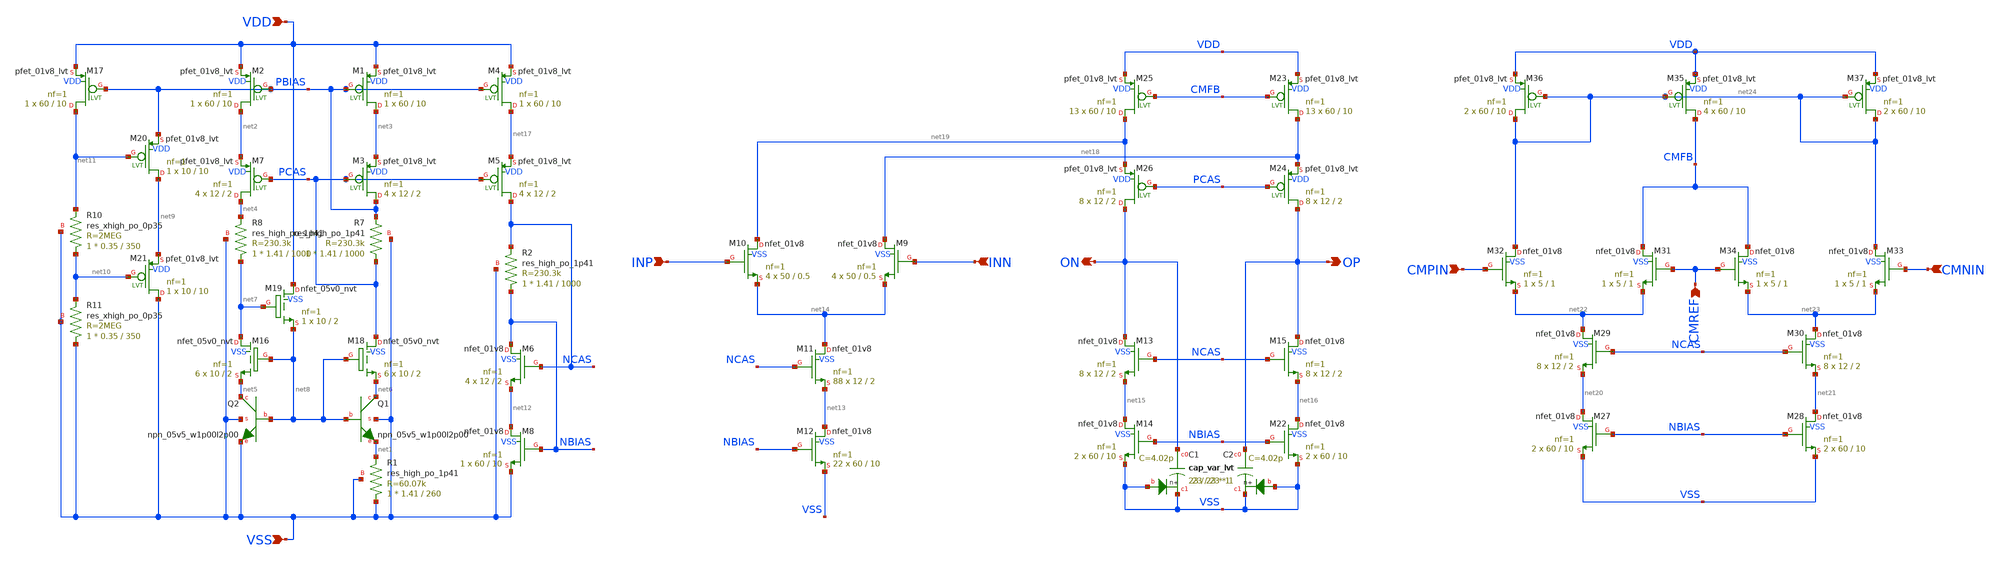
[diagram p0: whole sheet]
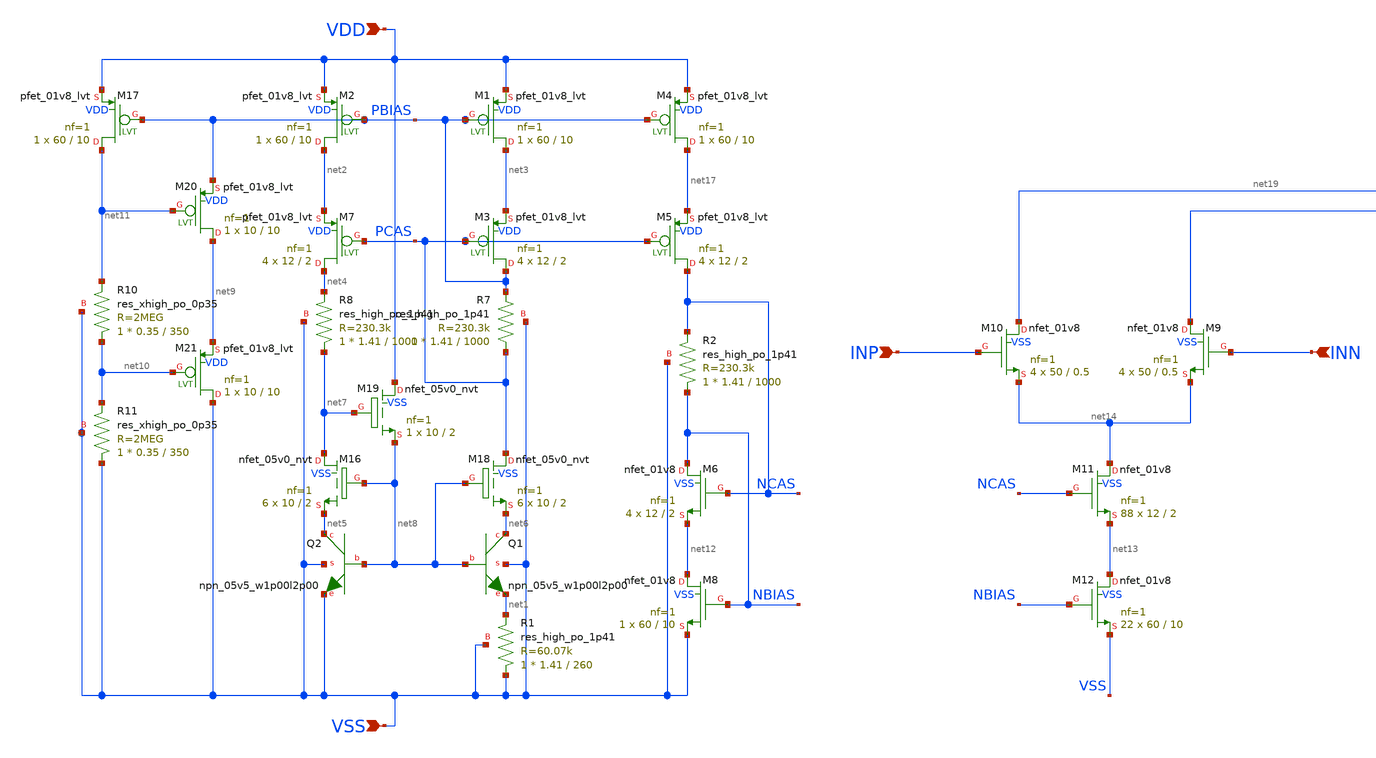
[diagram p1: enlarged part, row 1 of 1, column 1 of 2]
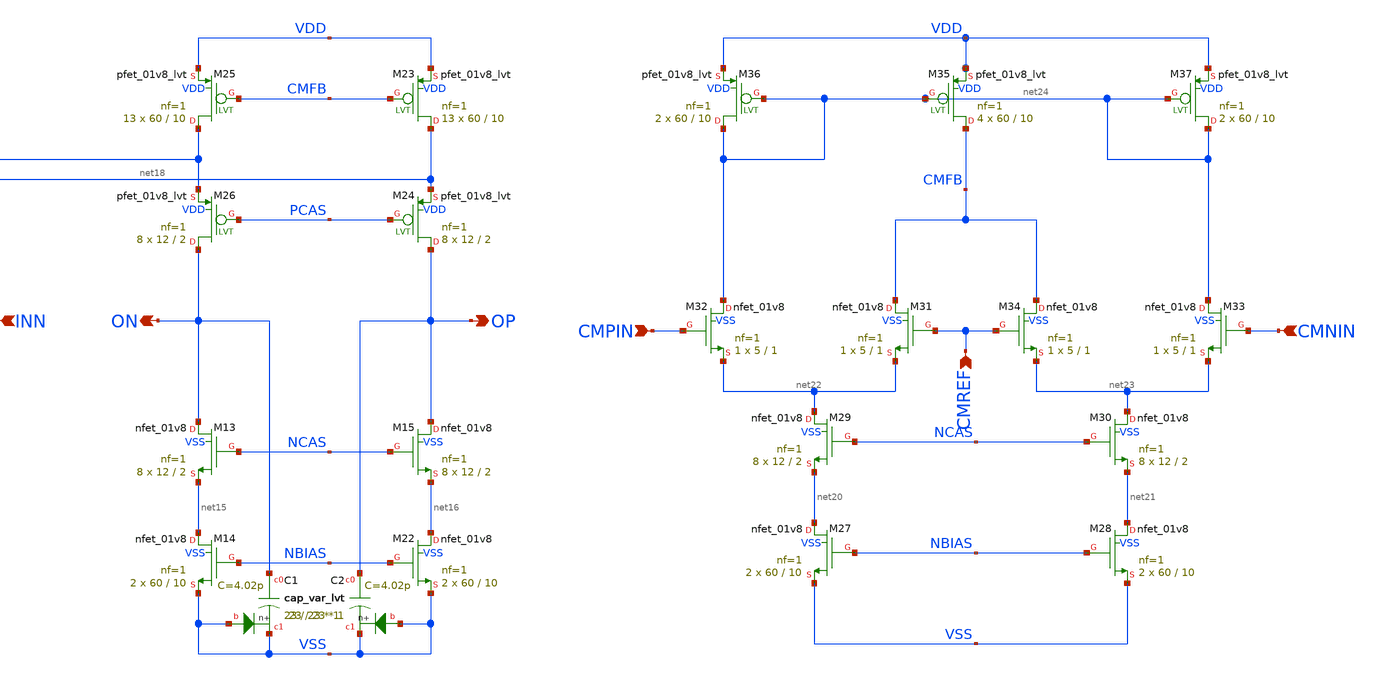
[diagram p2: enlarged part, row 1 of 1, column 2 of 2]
** sch_path: designs/fully_differential_amplifier.sch
**.subckt fully_differential_amplifier INP INN VDD VSS OP ON CMPIN CMNIN CMREF
*.ipin INP
*.ipin INN
*.ipin VDD
*.ipin VSS
*.opin OP
*.opin ON
*.ipin CMPIN
*.ipin CMNIN
*.ipin CMREF
XM1 net3 PBIAS VDD VDD sky130_fd_pr__pfet_01v8_lvt L=10 W=60 nf=1 ad='int((nf+1)/2) * W/nf * 0.29' as='int((nf+2)/2) * W/nf * 0.29'
+ pd='2*int((nf+1)/2) * (W/nf + 0.29)' ps='2*int((nf+2)/2) * (W/nf + 0.29)' nrd='0.29 / W' nrs='0.29 / W'
+ sa=0 sb=0 sd=0 mult=1 m=1
XM2 net2 PBIAS VDD VDD sky130_fd_pr__pfet_01v8_lvt L=10 W=60 nf=1 ad='int((nf+1)/2) * W/nf * 0.29' as='int((nf+2)/2) * W/nf * 0.29'
+ pd='2*int((nf+1)/2) * (W/nf + 0.29)' ps='2*int((nf+2)/2) * (W/nf + 0.29)' nrd='0.29 / W' nrs='0.29 / W'
+ sa=0 sb=0 sd=0 mult=1 m=1
XQ1 net6 net8 net1 VSS sky130_fd_pr__npn_05v5_w1p00l2p00
XQ2 net5 net8 VSS VSS sky130_fd_pr__npn_05v5_w1p00l2p00
XR1 VSS net1 VSS sky130_fd_pr__res_high_po_1p41 L=260 mult=1 m=1
XM3 PBIAS PCAS net3 VDD sky130_fd_pr__pfet_01v8_lvt L=2 W=12 nf=1 ad='int((nf+1)/2) * W/nf * 0.29' as='int((nf+2)/2) * W/nf * 0.29'
+ pd='2*int((nf+1)/2) * (W/nf + 0.29)' ps='2*int((nf+2)/2) * (W/nf + 0.29)' nrd='0.29 / W' nrs='0.29 / W'
+ sa=0 sb=0 sd=0 mult=4 m=4
XM7 net4 PCAS net2 VDD sky130_fd_pr__pfet_01v8_lvt L=2 W=12 nf=1 ad='int((nf+1)/2) * W/nf * 0.29' as='int((nf+2)/2) * W/nf * 0.29'
+ pd='2*int((nf+1)/2) * (W/nf + 0.29)' ps='2*int((nf+2)/2) * (W/nf + 0.29)' nrd='0.29 / W' nrs='0.29 / W'
+ sa=0 sb=0 sd=0 mult=4 m=4
XR7 PCAS PBIAS VSS sky130_fd_pr__res_high_po_1p41 L=1000 mult=1 m=1
XR8 net7 net4 VSS sky130_fd_pr__res_high_po_1p41 L=1000 mult=1 m=1
XM16 net7 net8 net5 VSS sky130_fd_pr__nfet_05v0_nvt L=2 W=10 nf=1 ad='int((nf+1)/2) * W/nf * 0.29' as='int((nf+2)/2) * W/nf * 0.29'
+ pd='2*int((nf+1)/2) * (W/nf + 0.29)' ps='2*int((nf+2)/2) * (W/nf + 0.29)' nrd='0.29 / W' nrs='0.29 / W'
+ sa=0 sb=0 sd=0 mult=6 m=6
XM18 PCAS net8 net6 VSS sky130_fd_pr__nfet_05v0_nvt L=2 W=10 nf=1 ad='int((nf+1)/2) * W/nf * 0.29' as='int((nf+2)/2) * W/nf * 0.29'
+ pd='2*int((nf+1)/2) * (W/nf + 0.29)' ps='2*int((nf+2)/2) * (W/nf + 0.29)' nrd='0.29 / W' nrs='0.29 / W'
+ sa=0 sb=0 sd=0 mult=6 m=6
XM19 VDD net7 net8 VSS sky130_fd_pr__nfet_05v0_nvt L=2 W=10 nf=1 ad='int((nf+1)/2) * W/nf * 0.29' as='int((nf+2)/2) * W/nf * 0.29'
+ pd='2*int((nf+1)/2) * (W/nf + 0.29)' ps='2*int((nf+2)/2) * (W/nf + 0.29)' nrd='0.29 / W' nrs='0.29 / W'
+ sa=0 sb=0 sd=0 mult=1 m=1
XM17 net11 PBIAS VDD VDD sky130_fd_pr__pfet_01v8_lvt L=10 W=60 nf=1 ad='int((nf+1)/2) * W/nf * 0.29'
+ as='int((nf+2)/2) * W/nf * 0.29' pd='2*int((nf+1)/2) * (W/nf + 0.29)' ps='2*int((nf+2)/2) * (W/nf + 0.29)'
+ nrd='0.29 / W' nrs='0.29 / W' sa=0 sb=0 sd=0 mult=1 m=1
XM20 net9 net11 PBIAS VDD sky130_fd_pr__pfet_01v8_lvt L=10 W=10 nf=1 ad='int((nf+1)/2) * W/nf * 0.29'
+ as='int((nf+2)/2) * W/nf * 0.29' pd='2*int((nf+1)/2) * (W/nf + 0.29)' ps='2*int((nf+2)/2) * (W/nf + 0.29)'
+ nrd='0.29 / W' nrs='0.29 / W' sa=0 sb=0 sd=0 mult=1 m=1
XM21 VSS net10 net9 VDD sky130_fd_pr__pfet_01v8_lvt L=10 W=10 nf=1 ad='int((nf+1)/2) * W/nf * 0.29' as='int((nf+2)/2) * W/nf * 0.29'
+ pd='2*int((nf+1)/2) * (W/nf + 0.29)' ps='2*int((nf+2)/2) * (W/nf + 0.29)' nrd='0.29 / W' nrs='0.29 / W'
+ sa=0 sb=0 sd=0 mult=1 m=1
XR10 net10 net11 VSS sky130_fd_pr__res_xhigh_po_0p35 L=350 mult=1 m=1
XR11 VSS net10 VSS sky130_fd_pr__res_xhigh_po_0p35 L=350 mult=1 m=1
XM4 net17 PBIAS VDD VDD sky130_fd_pr__pfet_01v8_lvt L=10 W=60 nf=1 ad='int((nf+1)/2) * W/nf * 0.29' as='int((nf+2)/2) * W/nf * 0.29'
+ pd='2*int((nf+1)/2) * (W/nf + 0.29)' ps='2*int((nf+2)/2) * (W/nf + 0.29)' nrd='0.29 / W' nrs='0.29 / W'
+ sa=0 sb=0 sd=0 mult=1 m=1
XM5 NCAS PCAS net17 VDD sky130_fd_pr__pfet_01v8_lvt L=2 W=12 nf=1 ad='int((nf+1)/2) * W/nf * 0.29' as='int((nf+2)/2) * W/nf * 0.29'
+ pd='2*int((nf+1)/2) * (W/nf + 0.29)' ps='2*int((nf+2)/2) * (W/nf + 0.29)' nrd='0.29 / W' nrs='0.29 / W'
+ sa=0 sb=0 sd=0 mult=4 m=4
XR2 NBIAS NCAS VSS sky130_fd_pr__res_high_po_1p41 L=1000 mult=1 m=1
XM6 NBIAS NCAS net12 VSS sky130_fd_pr__nfet_01v8 L=2 W=12 nf=1 ad='int((nf+1)/2) * W/nf * 0.29' as='int((nf+2)/2) * W/nf * 0.29'
+ pd='2*int((nf+1)/2) * (W/nf + 0.29)' ps='2*int((nf+2)/2) * (W/nf + 0.29)' nrd='0.29 / W' nrs='0.29 / W'
+ sa=0 sb=0 sd=0 mult=4 m=4
XM8 net12 NBIAS VSS VSS sky130_fd_pr__nfet_01v8 L=10 W=60 nf=1 ad='int((nf+1)/2) * W/nf * 0.29' as='int((nf+2)/2) * W/nf * 0.29'
+ pd='2*int((nf+1)/2) * (W/nf + 0.29)' ps='2*int((nf+2)/2) * (W/nf + 0.29)' nrd='0.29 / W' nrs='0.29 / W'
+ sa=0 sb=0 sd=0 mult=1 m=1
XM9 net18 INN net14 VSS sky130_fd_pr__nfet_01v8 L=0.5 W=50 nf=1 ad='int((nf+1)/2) * W/nf * 0.29' as='int((nf+2)/2) * W/nf * 0.29'
+ pd='2*int((nf+1)/2) * (W/nf + 0.29)' ps='2*int((nf+2)/2) * (W/nf + 0.29)' nrd='0.29 / W' nrs='0.29 / W'
+ sa=0 sb=0 sd=0 mult=4 m=4
XM10 net19 INP net14 VSS sky130_fd_pr__nfet_01v8 L=0.5 W=50 nf=1 ad='int((nf+1)/2) * W/nf * 0.29' as='int((nf+2)/2) * W/nf * 0.29'
+ pd='2*int((nf+1)/2) * (W/nf + 0.29)' ps='2*int((nf+2)/2) * (W/nf + 0.29)' nrd='0.29 / W' nrs='0.29 / W'
+ sa=0 sb=0 sd=0 mult=4 m=4
XM11 net14 NCAS net13 VSS sky130_fd_pr__nfet_01v8 L=2 W=12 nf=1 ad='int((nf+1)/2) * W/nf * 0.29' as='int((nf+2)/2) * W/nf * 0.29'
+ pd='2*int((nf+1)/2) * (W/nf + 0.29)' ps='2*int((nf+2)/2) * (W/nf + 0.29)' nrd='0.29 / W' nrs='0.29 / W'
+ sa=0 sb=0 sd=0 mult=88 m=88
XM12 net13 NBIAS VSS VSS sky130_fd_pr__nfet_01v8 L=10 W=60 nf=1 ad='int((nf+1)/2) * W/nf * 0.29' as='int((nf+2)/2) * W/nf * 0.29'
+ pd='2*int((nf+1)/2) * (W/nf + 0.29)' ps='2*int((nf+2)/2) * (W/nf + 0.29)' nrd='0.29 / W' nrs='0.29 / W'
+ sa=0 sb=0 sd=0 mult=22 m=22
XM13 ON NCAS net15 VSS sky130_fd_pr__nfet_01v8 L=2 W=12 nf=1 ad='int((nf+1)/2) * W/nf * 0.29' as='int((nf+2)/2) * W/nf * 0.29'
+ pd='2*int((nf+1)/2) * (W/nf + 0.29)' ps='2*int((nf+2)/2) * (W/nf + 0.29)' nrd='0.29 / W' nrs='0.29 / W'
+ sa=0 sb=0 sd=0 mult=8 m=8
XM14 net15 NBIAS VSS VSS sky130_fd_pr__nfet_01v8 L=10 W=60 nf=1 ad='int((nf+1)/2) * W/nf * 0.29' as='int((nf+2)/2) * W/nf * 0.29'
+ pd='2*int((nf+1)/2) * (W/nf + 0.29)' ps='2*int((nf+2)/2) * (W/nf + 0.29)' nrd='0.29 / W' nrs='0.29 / W'
+ sa=0 sb=0 sd=0 mult=2 m=2
XM15 OP NCAS net16 VSS sky130_fd_pr__nfet_01v8 L=2 W=12 nf=1 ad='int((nf+1)/2) * W/nf * 0.29' as='int((nf+2)/2) * W/nf * 0.29'
+ pd='2*int((nf+1)/2) * (W/nf + 0.29)' ps='2*int((nf+2)/2) * (W/nf + 0.29)' nrd='0.29 / W' nrs='0.29 / W'
+ sa=0 sb=0 sd=0 mult=8 m=8
XM22 net16 NBIAS VSS VSS sky130_fd_pr__nfet_01v8 L=10 W=60 nf=1 ad='int((nf+1)/2) * W/nf * 0.29' as='int((nf+2)/2) * W/nf * 0.29'
+ pd='2*int((nf+1)/2) * (W/nf + 0.29)' ps='2*int((nf+2)/2) * (W/nf + 0.29)' nrd='0.29 / W' nrs='0.29 / W'
+ sa=0 sb=0 sd=0 mult=2 m=2
XM23 net18 CMFB VDD VDD sky130_fd_pr__pfet_01v8_lvt L=10 W=60 nf=1 ad='int((nf+1)/2) * W/nf * 0.29' as='int((nf+2)/2) * W/nf * 0.29'
+ pd='2*int((nf+1)/2) * (W/nf + 0.29)' ps='2*int((nf+2)/2) * (W/nf + 0.29)' nrd='0.29 / W' nrs='0.29 / W'
+ sa=0 sb=0 sd=0 mult=13 m=13
XM24 OP PCAS net18 VDD sky130_fd_pr__pfet_01v8_lvt L=2 W=12 nf=1 ad='int((nf+1)/2) * W/nf * 0.29' as='int((nf+2)/2) * W/nf * 0.29'
+ pd='2*int((nf+1)/2) * (W/nf + 0.29)' ps='2*int((nf+2)/2) * (W/nf + 0.29)' nrd='0.29 / W' nrs='0.29 / W'
+ sa=0 sb=0 sd=0 mult=8 m=8
XM25 net19 CMFB VDD VDD sky130_fd_pr__pfet_01v8_lvt L=10 W=60 nf=1 ad='int((nf+1)/2) * W/nf * 0.29' as='int((nf+2)/2) * W/nf * 0.29'
+ pd='2*int((nf+1)/2) * (W/nf + 0.29)' ps='2*int((nf+2)/2) * (W/nf + 0.29)' nrd='0.29 / W' nrs='0.29 / W'
+ sa=0 sb=0 sd=0 mult=13 m=13
XM26 ON PCAS net19 VDD sky130_fd_pr__pfet_01v8_lvt L=2 W=12 nf=1 ad='int((nf+1)/2) * W/nf * 0.29' as='int((nf+2)/2) * W/nf * 0.29'
+ pd='2*int((nf+1)/2) * (W/nf + 0.29)' ps='2*int((nf+2)/2) * (W/nf + 0.29)' nrd='0.29 / W' nrs='0.29 / W'
+ sa=0 sb=0 sd=0 mult=8 m=8
XM27 net20 NBIAS VSS VSS sky130_fd_pr__nfet_01v8 L=10 W=60 nf=1 ad='int((nf+1)/2) * W/nf * 0.29' as='int((nf+2)/2) * W/nf * 0.29'
+ pd='2*int((nf+1)/2) * (W/nf + 0.29)' ps='2*int((nf+2)/2) * (W/nf + 0.29)' nrd='0.29 / W' nrs='0.29 / W'
+ sa=0 sb=0 sd=0 mult=2 m=2
XM28 net21 NBIAS VSS VSS sky130_fd_pr__nfet_01v8 L=10 W=60 nf=1 ad='int((nf+1)/2) * W/nf * 0.29' as='int((nf+2)/2) * W/nf * 0.29'
+ pd='2*int((nf+1)/2) * (W/nf + 0.29)' ps='2*int((nf+2)/2) * (W/nf + 0.29)' nrd='0.29 / W' nrs='0.29 / W'
+ sa=0 sb=0 sd=0 mult=2 m=2
XM29 net22 NCAS net20 VSS sky130_fd_pr__nfet_01v8 L=2 W=12 nf=1 ad='int((nf+1)/2) * W/nf * 0.29' as='int((nf+2)/2) * W/nf * 0.29'
+ pd='2*int((nf+1)/2) * (W/nf + 0.29)' ps='2*int((nf+2)/2) * (W/nf + 0.29)' nrd='0.29 / W' nrs='0.29 / W'
+ sa=0 sb=0 sd=0 mult=8 m=8
XM30 net23 NCAS net21 VSS sky130_fd_pr__nfet_01v8 L=2 W=12 nf=1 ad='int((nf+1)/2) * W/nf * 0.29' as='int((nf+2)/2) * W/nf * 0.29'
+ pd='2*int((nf+1)/2) * (W/nf + 0.29)' ps='2*int((nf+2)/2) * (W/nf + 0.29)' nrd='0.29 / W' nrs='0.29 / W'
+ sa=0 sb=0 sd=0 mult=8 m=8
XM31 CMFB CMREF net22 VSS sky130_fd_pr__nfet_01v8 L=1 W=5 nf=1 ad='int((nf+1)/2) * W/nf * 0.29' as='int((nf+2)/2) * W/nf * 0.29'
+ pd='2*int((nf+1)/2) * (W/nf + 0.29)' ps='2*int((nf+2)/2) * (W/nf + 0.29)' nrd='0.29 / W' nrs='0.29 / W'
+ sa=0 sb=0 sd=0 mult=1 m=1
XM32 net24 CMPIN net22 VSS sky130_fd_pr__nfet_01v8 L=1 W=5 nf=1 ad='int((nf+1)/2) * W/nf * 0.29' as='int((nf+2)/2) * W/nf * 0.29'
+ pd='2*int((nf+1)/2) * (W/nf + 0.29)' ps='2*int((nf+2)/2) * (W/nf + 0.29)' nrd='0.29 / W' nrs='0.29 / W'
+ sa=0 sb=0 sd=0 mult=1 m=1
XM33 net24 CMNIN net23 VSS sky130_fd_pr__nfet_01v8 L=1 W=5 nf=1 ad='int((nf+1)/2) * W/nf * 0.29' as='int((nf+2)/2) * W/nf * 0.29'
+ pd='2*int((nf+1)/2) * (W/nf + 0.29)' ps='2*int((nf+2)/2) * (W/nf + 0.29)' nrd='0.29 / W' nrs='0.29 / W'
+ sa=0 sb=0 sd=0 mult=1 m=1
XM34 CMFB CMREF net23 VSS sky130_fd_pr__nfet_01v8 L=1 W=5 nf=1 ad='int((nf+1)/2) * W/nf * 0.29' as='int((nf+2)/2) * W/nf * 0.29'
+ pd='2*int((nf+1)/2) * (W/nf + 0.29)' ps='2*int((nf+2)/2) * (W/nf + 0.29)' nrd='0.29 / W' nrs='0.29 / W'
+ sa=0 sb=0 sd=0 mult=1 m=1
XM35 CMFB net24 VDD VDD sky130_fd_pr__pfet_01v8_lvt L=10 W=60 nf=1 ad='int((nf+1)/2) * W/nf * 0.29' as='int((nf+2)/2) * W/nf * 0.29'
+ pd='2*int((nf+1)/2) * (W/nf + 0.29)' ps='2*int((nf+2)/2) * (W/nf + 0.29)' nrd='0.29 / W' nrs='0.29 / W'
+ sa=0 sb=0 sd=0 mult=4 m=4
XM36 net24 net24 VDD VDD sky130_fd_pr__pfet_01v8_lvt L=10 W=60 nf=1 ad='int((nf+1)/2) * W/nf * 0.29'
+ as='int((nf+2)/2) * W/nf * 0.29' pd='2*int((nf+1)/2) * (W/nf + 0.29)' ps='2*int((nf+2)/2) * (W/nf + 0.29)'
+ nrd='0.29 / W' nrs='0.29 / W' sa=0 sb=0 sd=0 mult=2 m=2
XM37 net24 net24 VDD VDD sky130_fd_pr__pfet_01v8_lvt L=10 W=60 nf=1 ad='int((nf+1)/2) * W/nf * 0.29'
+ as='int((nf+2)/2) * W/nf * 0.29' pd='2*int((nf+1)/2) * (W/nf + 0.29)' ps='2*int((nf+2)/2) * (W/nf + 0.29)'
+ nrd='0.29 / W' nrs='0.29 / W' sa=0 sb=0 sd=0 mult=2 m=2
XC1 ON VSS VSS sky130_fd_pr__cap_var_lvt W=23 L=23 VM=1 m=1
XC2 OP VSS VSS sky130_fd_pr__cap_var_lvt W=23 L=23 VM=1 m=1
**.ends
.end
